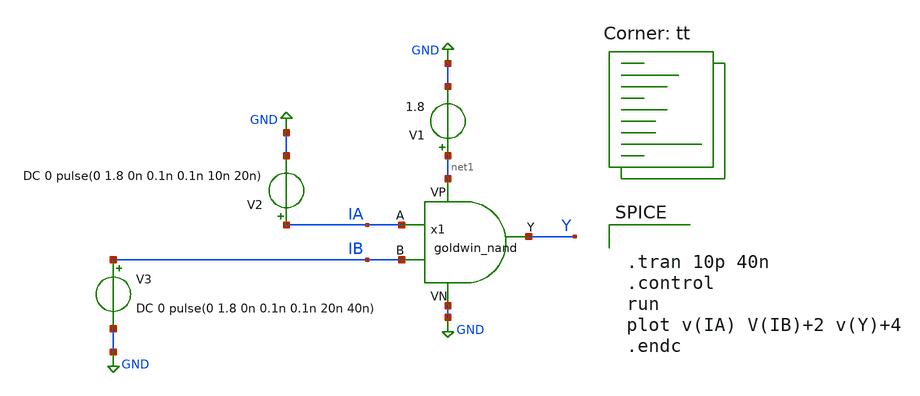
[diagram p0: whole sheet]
** sch_path: APIC-UTS/schematic/goldwin_nand/tb_goldwin_nand.sch
**.subckt tb_goldwin_nand
V1 net1 GND 1.8
V2 IA GND DC 0 pulse(0 1.8 0n 0.1n 0.1n 10n 20n)
x1 IA IB Y net1 GND goldwin_nand
V3 IB GND DC 0 pulse(0 1.8 0n 0.1n 0.1n 20n 40n)
**** begin user architecture code


.tran 10p 40n
.control
run
plot v(IA) V(IB)+2 v(Y)+4
.endc


.lib $::SKYWATER_MODELS/sky130.lib.spice tt
**** end user architecture code
**.ends
.GLOBAL GND
.end
